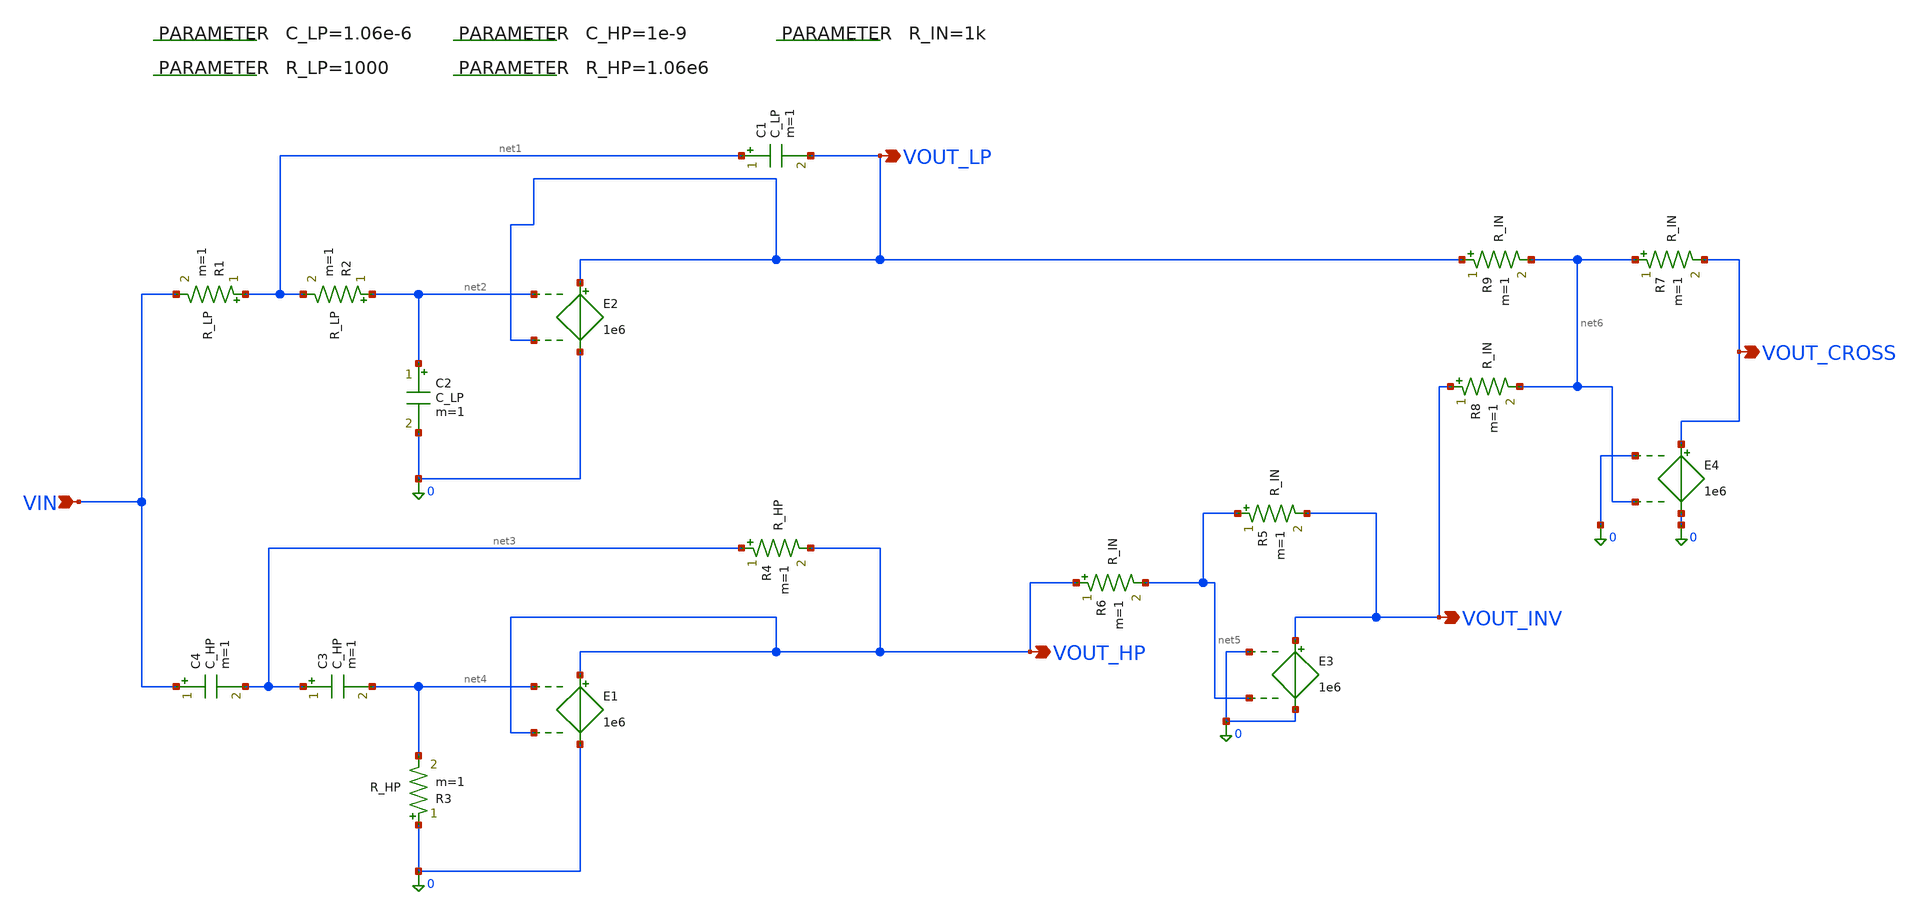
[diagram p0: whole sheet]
** sch_path: 003_Ideal_Circuits/linkwitz_riley_cross_vsvc_150hz.sch
**.subckt linkwitz_riley_cross_vsvc_150hz VIN VOUT_LP VOUT_HP VOUT_INV VOUT_CROSS
*.ipin VIN
*.opin VOUT_LP
*.opin VOUT_HP
*.opin VOUT_INV
*.opin VOUT_CROSS
R1 net1 VIN R_LP m=1
R2 net2 net1 R_LP m=1
C1 net1 VOUT_LP C_LP m=1
C2 net2 0 C_LP m=1
.param C_LP=1.06e-6
.param R_LP=1000
R3 0 net4 R_HP m=1
R4 net3 VOUT_HP R_HP m=1
C3 net3 net4 C_HP m=1
C4 VIN net3 C_HP m=1
.param C_HP=1e-9
.param R_HP=1.06e6
R5 net5 VOUT_INV R_IN m=1
R6 VOUT_HP net5 R_IN m=1
.param R_IN=1k
R7 net6 VOUT_CROSS R_IN m=1
R8 VOUT_INV net6 R_IN m=1
R9 VOUT_LP net6 R_IN m=1
E2 VOUT_LP 0 net2 VOUT_LP 1e6
E1 VOUT_HP 0 net4 VOUT_HP 1e6
E3 VOUT_INV 0 0 net5 1e6
E4 VOUT_CROSS 0 0 net6 1e6
**.ends
.end
